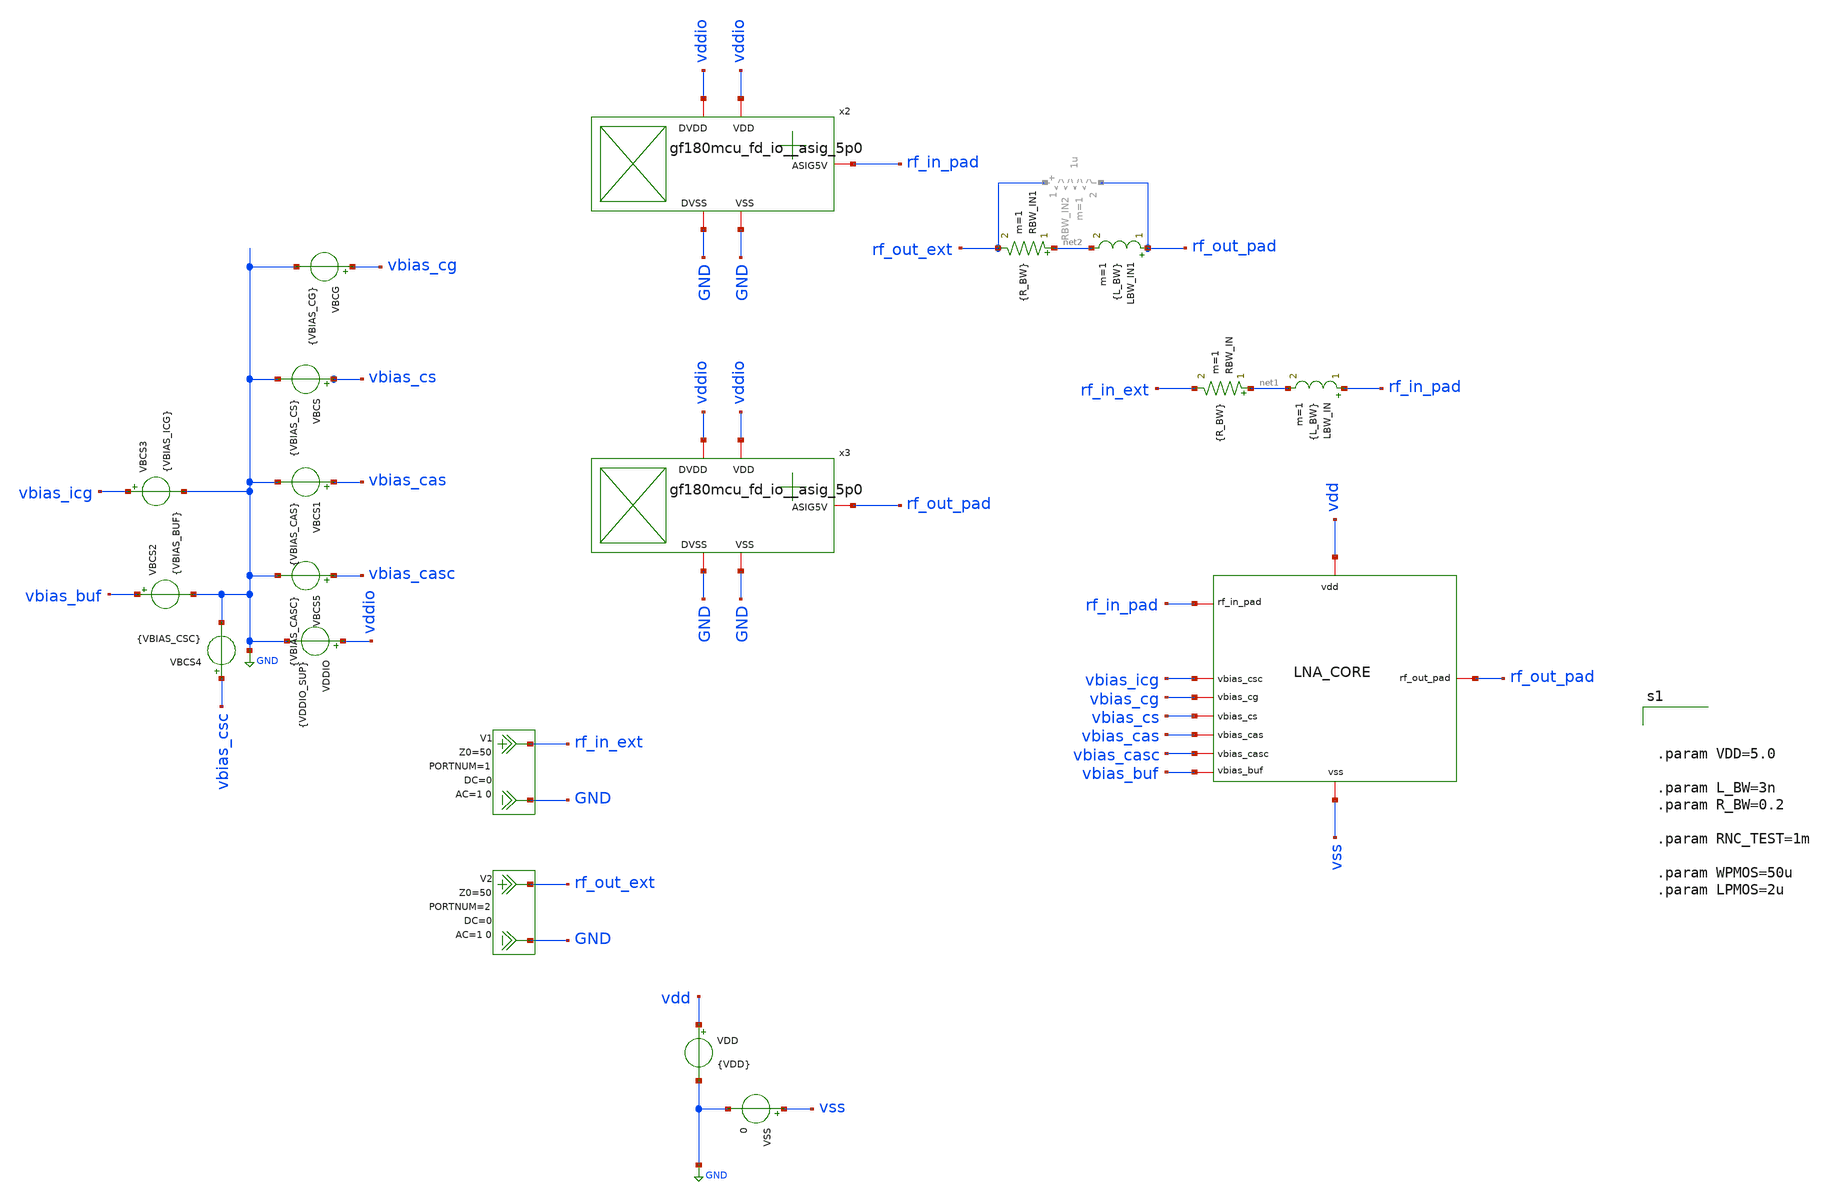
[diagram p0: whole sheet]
** sch_path: xschem/lna-core_tb.sch
**.subckt lna-core_tb
x1 vbias_cg rf_in_pad vbias_cs rf_out_pad vdd vbias_cas vss vbias_casc vbias_buf vbias_icg lna_core
VDD vdd GND {VDD}
VSS vss GND 0
LBW_IN rf_in_pad net1 {L_BW} m=1
RBW_IN net1 rf_in_ext {R_BW} m=1
LBW_IN1 rf_out_pad net2 {L_BW} m=1
RBW_IN1 net2 rf_out_ext {R_BW} m=1
VBCG vbias_cg GND {VBIAS_CG}
VDDIO vddio GND {VDDIO_SUP}
VBCS vbias_cs GND {VBIAS_CS}
VBCS1 vbias_cas GND {VBIAS_CAS}
VBCS2 vbias_buf GND {VBIAS_BUF}
VBCS3 vbias_icg GND {VBIAS_ICG}
VBCS4 vbias_csc GND {VBIAS_CSC}
VBCS5 vbias_casc GND {VBIAS_CASC}
V1 rf_in_ext GND DC 0 AC 1 0 portnum 1 z0 50
V2 rf_out_ext GND DC 0 AC 1 0 portnum 2 z0 50
x2 rf_in_pad vddio GND vddio GND gf180mcu_fd_io__asig_5p0
x3 rf_out_pad vddio GND vddio GND gf180mcu_fd_io__asig_5p0
**** begin user architecture code

.include $::180MCU_MODELS/design.ngspice
.lib $::180MCU_MODELS/sm141064.ngspice typical
.lib $::180MCU_MODELS/sm141064.ngspice cap_mim
.lib $::180MCU_MODELS/sm141064.ngspice res_typical
.lib $::180MCU_MODELS/sm141064.ngspice moscap_typical
.lib $::180MCU_MODELS/sm141064.ngspice mimcap_typical
.lib $::180MCU_MODELS/sm141064.ngspice diode_typical

.include $::env(PWD)/gf180mcu_fd_io__asig_5p0_pex__pdk_gf180mcuD__rcx__flat__cthresh_0__extresist_0mohm.spice

* ============================================================
* INDUCTOR MODEL SWEEP CONFIG -- change the shared section name
* (ideal / rl / snp2le) in all 4 lines below to switch every
* swept inductor's model at once, or run:
*   ./set_inductor_model.sh ideal_or_rl_or_snp2le
* from the xschem/ directory.
*   ideal  : single ideal inductor (L only)
*   rl     : EM-derived series L + equivalent series R
*   snp2le : snp2le broadband vector-fitted macromodel (passive,
*            DC-pinned, thermal-noise-synthesized), same EM data as rl
* ============================================================
.lib $::env(PWD)/LEQ_model.lib rl
.lib $::env(PWD)/LSHUNT_OUT_model.lib rl
.lib $::env(PWD)/LD2_model.lib rl
.lib $::env(PWD)/LD4_model.lib rl




.param VDD=5.0

.param L_BW=3n
.param R_BW=0.2

.param RNC_TEST=1m

.param WPMOS=50u
.param LPMOS=2u






.control

set noaskquit
set wr_singlescale
set wr_vecnames
set numdgt=10

let target_gain_bw=10.0

echo ============================================================ > lna_core_06V_cgcs_report.txt
echo GF180MCU_LNA_CORE_06V_CGCS_DETAILED_REPORT >> lna_core_06V_cgcs_report.txt
echo TARGET_FREQUENCY_HZ 2.400e9 >> lna_core_06V_cgcs_report.txt
echo TARGET_BAND_HZ 2.300e9 2.500e9 >> lna_core_06V_cgcs_report.txt
echo GAIN_BANDWIDTH_THRESHOLD_DB 10.0 >> lna_core_06V_cgcs_report.txt
echo PORT_REFERENCE_OHM 50 >> lna_core_06V_cgcs_report.txt
echo NOTE_HIERARCHY LNA_CORE_INSTANCE_IS_X1 >> lna_core_06V_cgcs_report.txt
echo ============================================================ >> lna_core_06V_cgcs_report.txt

* =============================================================================
* DC OPERATING POINT
* =============================================================================

op

* Top-level supply and bias-generator values.
let pdcop=1e3*abs(i(VDD))*v(vdd)
let icoreop=abs(i(VDD))
let iioop=0

let v_vddop=v(vdd)
let v_vpop=v(vp)
let v_vrefop=v(vref)
let v_vsenseop=v(vsense)
let v_vbias_casop=v(vbias_cas)
let v_vbias_3v3op=v(vbias_3v3)
let v_vbias_cascop=v(vbias_casc)
let v_vbias_cgop=v(vbias_cg)
let v_vbias_icgop=v(vbias_icg)
let v_vbias_bufop=v(vbias_buf)
let v_vbias_csop=v(vbias_cs)
let v_vbias_cscop=v(vbias_csc)

let i_r1=(v(vbias_cas)-v(vbias_3v3))/20k
let i_r2=(v(vbias_3v3)-v(vbias_casc))/5k
let i_r3=(v(vbias_casc)-v(vbias_cg))/50k
let i_r4=(v(vbias_cg)-v(vbias_icg))/15k
let i_r5=(v(vbias_icg)-v(vbias_buf))/30k
let i_r6=(v(vbias_buf)-v(vbias_cs))/5k
let i_r7=(v(vbias_cs)-v(vsense))/3.066k
let i_r8=(v(vsense)-v(vbias_csc))/11.934k
let i_r9=v(vbias_csc)/45k
let i_ladder_avg=(i_r1+i_r2+i_r3+i_r4+i_r5+i_r6+i_r7+i_r8+i_r9)/9

* LNA internal nodes are inside instance x1.
let vsop=v(x1.s)
let vdop=v(x1.vm2)
let vnet3op=v(x1.net3)
let vnet8op=v(x1.net8)
let vbufop=v(x1.vbuf)
let vgcsop=v(x1.g_cs)
let vgcgop=v(x1.g_cg)
let vgcsccop=v(x1.g_csc)
let vxop=v(x1.vx)
let vm1op=v(x1.vm1)
let vm2op=v(x1.vm2)

* XM1: main CS device.
let id1op=abs(@m.x1.xm1.m0[id])
let gm1op=@m.x1.xm1.m0[gm]
let gmb1op=@m.x1.xm1.m0[gmbs]
let gds1op=@m.x1.xm1.m0[gds]
let vgs1op=@m.x1.xm1.m0[vgs]
let vds1op=@m.x1.xm1.m0[vds]
let vbs1op=@m.x1.xm1.m0[vbs]
let vth1op=@m.x1.xm1.m0[vth]
let vov1op=vgs1op-vth1op
let vdsat1op=abs(@m.x1.xm1.m0[vdsat])
let sat1op=vds1op-vdsat1op
let gmid1op=gm1op/(id1op+1e-30)
let ro1op=1/(gds1op+1e-30)

* XM2: CG input device.
let id2op=abs(@m.x1.xm2.m0[id])
let gm2op=@m.x1.xm2.m0[gm]
let gmb2op=@m.x1.xm2.m0[gmbs]
let gds2op=@m.x1.xm2.m0[gds]
let vgs2op=@m.x1.xm2.m0[vgs]
let vds2op=@m.x1.xm2.m0[vds]
let vbs2op=@m.x1.xm2.m0[vbs]
let vth2op=@m.x1.xm2.m0[vth]
let vov2op=vgs2op-vth2op
let vdsat2op=abs(@m.x1.xm2.m0[vdsat])
let sat2op=vds2op-vdsat2op
let gmid2op=gm2op/(id2op+1e-30)
let ro2op=1/(gds2op+1e-30)

* XM3: source follower.
let id3op=abs(@m.x1.xm3.m0[id])
let gm3op=@m.x1.xm3.m0[gm]
let gmb3op=@m.x1.xm3.m0[gmbs]
let gds3op=@m.x1.xm3.m0[gds]
let vgs3op=@m.x1.xm3.m0[vgs]
let vds3op=@m.x1.xm3.m0[vds]
let vbs3op=@m.x1.xm3.m0[vbs]
let vth3op=@m.x1.xm3.m0[vth]
let vov3op=vgs3op-vth3op
let vdsat3op=abs(@m.x1.xm3.m0[vdsat])
let sat3op=vds3op-vdsat3op
let gmid3op=gm3op/(id3op+1e-30)
let ro3op=1/(gds3op+1e-30)

* XM4: CS cascode.
let id4op=abs(@m.x1.xm4.m0[id])
let gm4op=@m.x1.xm4.m0[gm]
let gmb4op=@m.x1.xm4.m0[gmbs]
let gds4op=@m.x1.xm4.m0[gds]
let vgs4op=@m.x1.xm4.m0[vgs]
let vds4op=@m.x1.xm4.m0[vds]
let vbs4op=@m.x1.xm4.m0[vbs]
let vth4op=@m.x1.xm4.m0[vth]
let vov4op=vgs4op-vth4op
let vdsat4op=abs(@m.x1.xm4.m0[vdsat])
let sat4op=vds4op-vdsat4op
let gmid4op=gm4op/(id4op+1e-30)
let ro4op=1/(gds4op+1e-30)

* XM5: CG current sink.
let id5op=abs(@m.x1.xm5.m0[id])
let gm5op=@m.x1.xm5.m0[gm]
let gmb5op=@m.x1.xm5.m0[gmbs]
let gds5op=@m.x1.xm5.m0[gds]
let vgs5op=@m.x1.xm5.m0[vgs]
let vds5op=@m.x1.xm5.m0[vds]
let vbs5op=@m.x1.xm5.m0[vbs]
let vth5op=@m.x1.xm5.m0[vth]
let vov5op=vgs5op-vth5op
let vdsat5op=abs(@m.x1.xm5.m0[vdsat])
let sat5op=vds5op-vdsat5op
let gmid5op=gm5op/(id5op+1e-30)
let ro5op=1/(gds5op+1e-30)

* XM6: buffer current sink.
let id6op=abs(@m.x1.xm6.m0[id])
let gm6op=@m.x1.xm6.m0[gm]
let gmb6op=@m.x1.xm6.m0[gmbs]
let gds6op=@m.x1.xm6.m0[gds]
let vgs6op=@m.x1.xm6.m0[vgs]
let vds6op=@m.x1.xm6.m0[vds]
let vbs6op=@m.x1.xm6.m0[vbs]
let vth6op=@m.x1.xm6.m0[vth]
let vov6op=vgs6op-vth6op
let vdsat6op=abs(@m.x1.xm6.m0[vdsat])
let sat6op=vds6op-vdsat6op
let gmid6op=gm6op/(id6op+1e-30)
let ro6op=1/(gds6op+1e-30)

* XM7: CG cascode.
let id7op=abs(@m.x1.xm7.m0[id])
let gm7op=@m.x1.xm7.m0[gm]
let gmb7op=@m.x1.xm7.m0[gmbs]
let gds7op=@m.x1.xm7.m0[gds]
let vgs7op=@m.x1.xm7.m0[vgs]
let vds7op=@m.x1.xm7.m0[vds]
let vbs7op=@m.x1.xm7.m0[vbs]
let vth7op=@m.x1.xm7.m0[vth]
let vov7op=vgs7op-vth7op
let vdsat7op=abs(@m.x1.xm7.m0[vdsat])
let sat7op=vds7op-vdsat7op
let gmid7op=gm7op/(id7op+1e-30)
let ro7op=1/(gds7op+1e-30)

* XM9: cancellation CS.
let id9op=abs(@m.x1.xm9.m0[id])
let gm9op=@m.x1.xm9.m0[gm]
let gmb9op=@m.x1.xm9.m0[gmbs]
let gds9op=@m.x1.xm9.m0[gds]
let vgs9op=@m.x1.xm9.m0[vgs]
let vds9op=@m.x1.xm9.m0[vds]
let vbs9op=@m.x1.xm9.m0[vbs]
let vth9op=@m.x1.xm9.m0[vth]
let vov9op=vgs9op-vth9op
let vdsat9op=abs(@m.x1.xm9.m0[vdsat])
let sat9op=vds9op-vdsat9op
let gmid9op=gm9op/(id9op+1e-30)
let ro9op=1/(gds9op+1e-30)

let vnet9op=vnet3op+vds1op
let vnet9check=vnet8op-vds4op
let vnet9diff=vnet9op-vnet9check
let vnet10op=vsop+vds2op
let vnet10check=vdop-vds7op
let vnet10diff=vnet10op-vnet10check

set op_pdc=$&pdcop
set op_icore=$&icoreop
set op_iio=$&iioop
set op_vs=$&vsop
set op_vnet10=$&vnet10op
set op_vnet10check=$&vnet10check
set op_vnet10diff=$&vnet10diff
set op_vd=$&vdop
set op_vnet3=$&vnet3op
set op_vnet9=$&vnet9op
set op_vnet9check=$&vnet9check
set op_vnet9diff=$&vnet9diff
set op_vnet8=$&vnet8op
set op_vbuf=$&vbufop
set op_vgcs=$&vgcsop
set op_vgcg=$&vgcgop
set op_vgcsc=$&vgcsccop
set op_vx=$&vxop
set op_vm1=$&vm1op
set op_vm2=$&vm2op

set op_vdd=$&v_vddop
set op_vp=$&v_vpop
set op_vref=$&v_vrefop
set op_vsense=$&v_vsenseop
set op_vbias_cas=$&v_vbias_casop
set op_vbias_3v3=$&v_vbias_3v3op
set op_vbias_casc=$&v_vbias_cascop
set op_vbias_cg=$&v_vbias_cgop
set op_vbias_icg=$&v_vbias_icgop
set op_vbias_buf=$&v_vbias_bufop
set op_vbias_cs=$&v_vbias_csop
set op_vbias_csc=$&v_vbias_cscop
set op_iladder=$&i_ladder_avg

set op_id1=$&id1op
set op_gm1=$&gm1op
set op_gmb1=$&gmb1op
set op_gds1=$&gds1op
set op_vgs1=$&vgs1op
set op_vds1=$&vds1op
set op_vbs1=$&vbs1op
set op_vth1=$&vth1op
set op_vov1=$&vov1op
set op_vdsat1=$&vdsat1op
set op_sat1=$&sat1op
set op_gmid1=$&gmid1op
set op_ro1=$&ro1op

set op_id2=$&id2op
set op_gm2=$&gm2op
set op_gmb2=$&gmb2op
set op_gds2=$&gds2op
set op_vgs2=$&vgs2op
set op_vds2=$&vds2op
set op_vbs2=$&vbs2op
set op_vth2=$&vth2op
set op_vov2=$&vov2op
set op_vdsat2=$&vdsat2op
set op_sat2=$&sat2op
set op_gmid2=$&gmid2op
set op_ro2=$&ro2op

set op_id3=$&id3op
set op_gm3=$&gm3op
set op_gmb3=$&gmb3op
set op_gds3=$&gds3op
set op_vgs3=$&vgs3op
set op_vds3=$&vds3op
set op_vbs3=$&vbs3op
set op_vth3=$&vth3op
set op_vov3=$&vov3op
set op_vdsat3=$&vdsat3op
set op_sat3=$&sat3op
set op_gmid3=$&gmid3op
set op_ro3=$&ro3op

set op_id4=$&id4op
set op_gm4=$&gm4op
set op_gmb4=$&gmb4op
set op_gds4=$&gds4op
set op_vgs4=$&vgs4op
set op_vds4=$&vds4op
set op_vbs4=$&vbs4op
set op_vth4=$&vth4op
set op_vov4=$&vov4op
set op_vdsat4=$&vdsat4op
set op_sat4=$&sat4op
set op_gmid4=$&gmid4op
set op_ro4=$&ro4op

set op_id5=$&id5op
set op_gm5=$&gm5op
set op_gmb5=$&gmb5op
set op_gds5=$&gds5op
set op_vgs5=$&vgs5op
set op_vds5=$&vds5op
set op_vbs5=$&vbs5op
set op_vth5=$&vth5op
set op_vov5=$&vov5op
set op_vdsat5=$&vdsat5op
set op_sat5=$&sat5op
set op_gmid5=$&gmid5op
set op_ro5=$&ro5op

set op_id6=$&id6op
set op_gm6=$&gm6op
set op_gmb6=$&gmb6op
set op_gds6=$&gds6op
set op_vgs6=$&vgs6op
set op_vds6=$&vds6op
set op_vbs6=$&vbs6op
set op_vth6=$&vth6op
set op_vov6=$&vov6op
set op_vdsat6=$&vdsat6op
set op_sat6=$&sat6op
set op_gmid6=$&gmid6op
set op_ro6=$&ro6op

set op_id7=$&id7op
set op_gm7=$&gm7op
set op_gmb7=$&gmb7op
set op_gds7=$&gds7op
set op_vgs7=$&vgs7op
set op_vds7=$&vds7op
set op_vbs7=$&vbs7op
set op_vth7=$&vth7op
set op_vov7=$&vov7op
set op_vdsat7=$&vdsat7op
set op_sat7=$&sat7op
set op_gmid7=$&gmid7op
set op_ro7=$&ro7op

set op_id9=$&id9op
set op_gm9=$&gm9op
set op_gmb9=$&gmb9op
set op_gds9=$&gds9op
set op_vgs9=$&vgs9op
set op_vds9=$&vds9op
set op_vbs9=$&vbs9op
set op_vth9=$&vth9op
set op_vov9=$&vov9op
set op_vdsat9=$&vdsat9op
set op_sat9=$&sat9op
set op_gmid9=$&gmid9op
set op_ro9=$&ro9op

echo ============================================================ >> lna_core_06V_cgcs_report.txt
echo DC_SUPPLY_AND_BIAS_GENERATOR >> lna_core_06V_cgcs_report.txt
echo PDC_mW $op_pdc ICORE_A $op_icore IIO_A $op_iio >> lna_core_06V_cgcs_report.txt
echo BIAS_TOP_LEVEL_V VDD $op_vdd VP_BANDGAP $op_vp OTA_OUT_VREF $op_vref VSENSE $op_vsense ILADDER_A $op_iladder >> lna_core_06V_cgcs_report.txt
echo BIAS_LADDER_V VBIAS_CAS $op_vbias_cas VBIAS_3V3 $op_vbias_3v3 VBIAS_CASC $op_vbias_casc VBIAS_CG $op_vbias_cg VBIAS_ICG $op_vbias_icg VBIAS_BUF $op_vbias_buf VBIAS_CS $op_vbias_cs VBIAS_CSC $op_vbias_csc >> lna_core_06V_cgcs_report.txt
echo ============================================================ >> lna_core_06V_cgcs_report.txt
echo DC_LNA_INTERNAL_NODE_VOLTAGES >> lna_core_06V_cgcs_report.txt
echo NODES_V S $op_vs VX $op_vx VM1 $op_vm1 VM2 $op_vm2 NET10_DERIVED $op_vnet10 NET3 $op_vnet3 NET9_DERIVED $op_vnet9 NET8 $op_vnet8 VBUF $op_vbuf G_CS $op_vgcs G_CG $op_vgcg G_CSC $op_vgcsc >> lna_core_06V_cgcs_report.txt
echo HIDDEN_NODE_CHECKS NET10_FROM_XM2 $op_vnet10 NET10_FROM_XM7 $op_vnet10check DIFFERENCE $op_vnet10diff NET9_FROM_XM1 $op_vnet9 NET9_FROM_XM4 $op_vnet9check DIFFERENCE $op_vnet9diff >> lna_core_06V_cgcs_report.txt
echo ============================================================ >> lna_core_06V_cgcs_report.txt
echo TRANSISTOR_OPERATING_POINTS >> lna_core_06V_cgcs_report.txt
echo FIELDS ID_A GM_S GMBS_S GDS_S VGS_V VDS_V VBS_V VTH_V VOV_V VDSAT_V SAT_MARGIN_V GM_OVER_ID_1_PER_V RO_OHM >> lna_core_06V_cgcs_report.txt
echo XM1_CS ID $op_id1 GM $op_gm1 GMBS $op_gmb1 GDS $op_gds1 VGS $op_vgs1 VDS $op_vds1 VBS $op_vbs1 VTH $op_vth1 VOV $op_vov1 VDSAT $op_vdsat1 SAT_MARGIN $op_sat1 GMID $op_gmid1 RO $op_ro1 >> lna_core_06V_cgcs_report.txt
echo XM2_CG ID $op_id2 GM $op_gm2 GMBS $op_gmb2 GDS $op_gds2 VGS $op_vgs2 VDS $op_vds2 VBS $op_vbs2 VTH $op_vth2 VOV $op_vov2 VDSAT $op_vdsat2 SAT_MARGIN $op_sat2 GMID $op_gmid2 RO $op_ro2 >> lna_core_06V_cgcs_report.txt
echo XM3_SOURCE_FOLLOWER ID $op_id3 GM $op_gm3 GMBS $op_gmb3 GDS $op_gds3 VGS $op_vgs3 VDS $op_vds3 VBS $op_vbs3 VTH $op_vth3 VOV $op_vov3 VDSAT $op_vdsat3 SAT_MARGIN $op_sat3 GMID $op_gmid3 RO $op_ro3 >> lna_core_06V_cgcs_report.txt
echo XM4_CS_CASCODE ID $op_id4 GM $op_gm4 GMBS $op_gmb4 GDS $op_gds4 VGS $op_vgs4 VDS $op_vds4 VBS $op_vbs4 VTH $op_vth4 VOV $op_vov4 VDSAT $op_vdsat4 SAT_MARGIN $op_sat4 GMID $op_gmid4 RO $op_ro4 >> lna_core_06V_cgcs_report.txt
echo XM5_CG_CURRENT_SINK ID $op_id5 GM $op_gm5 GMBS $op_gmb5 GDS $op_gds5 VGS $op_vgs5 VDS $op_vds5 VBS $op_vbs5 VTH $op_vth5 VOV $op_vov5 VDSAT $op_vdsat5 SAT_MARGIN $op_sat5 GMID $op_gmid5 RO $op_ro5 >> lna_core_06V_cgcs_report.txt
echo XM6_BUFFER_CURRENT_SINK ID $op_id6 GM $op_gm6 GMBS $op_gmb6 GDS $op_gds6 VGS $op_vgs6 VDS $op_vds6 VBS $op_vbs6 VTH $op_vth6 VOV $op_vov6 VDSAT $op_vdsat6 SAT_MARGIN $op_sat6 GMID $op_gmid6 RO $op_ro6 >> lna_core_06V_cgcs_report.txt
echo XM7_CG_CASCODE ID $op_id7 GM $op_gm7 GMBS $op_gmb7 GDS $op_gds7 VGS $op_vgs7 VDS $op_vds7 VBS $op_vbs7 VTH $op_vth7 VOV $op_vov7 VDSAT $op_vdsat7 SAT_MARGIN $op_sat7 GMID $op_gmid7 RO $op_ro7 >> lna_core_06V_cgcs_report.txt
echo XM9_CANCELLATION_CS ID $op_id9 GM $op_gm9 GMBS $op_gmb9 GDS $op_gds9 VGS $op_vgs9 VDS $op_vds9 VBS $op_vbs9 VTH $op_vth9 VOV $op_vov9 VDSAT $op_sat9 SAT_MARGIN $op_sat9 GMID $op_gmid9 RO $op_ro9 >> lna_core_06V_cgcs_report.txt

destroy $curplot

* =============================================================================
* SINGLE BROADBAND RF ANALYSIS
* One reset and one SP run are used for all 1 MHz to 7 GHz RF results.
* Target-band values are extracted from the same dataset.
* =============================================================================

reset
sp lin 101 500Meg 5Gig 1
set rfplot=$curplot

let fghz=frequency/1e9

let s11db=db(s_1_1)
let s21db=db(s_2_1)
let s12db=db(s_1_2)
let s22db=db(s_2_2)

let s11re=real(s_1_1)
let s11im=imag(s_1_1)
let s21re=real(s_2_1)
let s21im=imag(s_2_1)
let s12re=real(s_1_2)
let s12im=imag(s_1_2)
let s22re=real(s_2_2)
let s22im=imag(s_2_2)

let z22re=real(z_2_2)
let z22im=imag(z_2_2)

let nfdb=real(NF)
let nfmin_db=real(NFmin)

let delta=s_1_1*s_2_2-s_1_2*s_2_1
let delta_mag=mag(delta)
let a11=mag(s_1_1)
let a12=mag(s_1_2)
let a21=mag(s_2_1)
let a22=mag(s_2_2)
let mu=(1-a11*a11)/(mag(s_2_2-delta*conj(s_1_1))+mag(s_1_2*s_2_1))
let mup=(1-a22*a22)/(mag(s_1_1-delta*conj(s_2_2))+mag(s_1_2*s_2_1))
let kval=(1-a11*a11-a22*a22+delta_mag*delta_mag)/(2*a12*a21)

let zin=50*(1+s_1_1)/(1-s_1_1)
let zout=50*(1+s_2_2)/(1-s_2_2)
let zin_re=real(zin)
let zin_im=imag(zin)
let zout_re=real(zout)
let zout_im=imag(zout)

let npts=length(frequency)

let ilo=0
let icenter=0
let ihi=0
let errlo=abs(frequency[0]-2.3e9)
let errcenter=abs(frequency[0]-2.4e9)
let errhi=abs(frequency[0]-2.5e9)
let ii=1

while ii < npts
let newerr=abs(frequency[ii]-2.3e9)
if newerr < errlo
let errlo=newerr
let ilo=ii
end
let newerr=abs(frequency[ii]-2.4e9)
if newerr < errcenter
let errcenter=newerr
let icenter=ii
end
let newerr=abs(frequency[ii]-2.5e9)
if newerr < errhi
let errhi=newerr
let ihi=ii
end
let ii=ii+1
end

let center_freq=frequency[icenter]
let s11c=s11db[icenter]
let s21c=s21db[icenter]
let s12c=s12db[icenter]
let s22c=s22db[icenter]
let s11rc=s11re[icenter]
let s11ic=s11im[icenter]
let s21rc=s21re[icenter]
let s21ic=s21im[icenter]
let s12rc=s12re[icenter]
let s12ic=s12im[icenter]
let s22rc=s22re[icenter]
let s22ic=s22im[icenter]
let nfc=nfdb[icenter]
let nfminc=nfmin_db[icenter]
let muc=mu[icenter]
let mupc=mup[icenter]
let kc=kval[icenter]
let dmc=delta_mag[icenter]
let zinrc=zin_re[icenter]
let zinic=zin_im[icenter]
let zoutrc=zout_re[icenter]
let zoutic=zout_im[icenter]

let s11min=s11db[ilo]
let s11max=s11db[ilo]
let s21min=s21db[ilo]
let s21max=s21db[ilo]
let s12min=s12db[ilo]
let s12max=s12db[ilo]
let s22min=s22db[ilo]
let s22max=s22db[ilo]
let nfbandmin=nfdb[ilo]
let nfbandmax=nfdb[ilo]
let nfminbandmin=nfmin_db[ilo]
let nfminbandmax=nfmin_db[ilo]
let mumin=mu[ilo]
let mupmin=mup[ilo]
let kmin=kval[ilo]
let dmax=delta_mag[ilo]

let s11min_i=ilo
let s11max_i=ilo
let s21min_i=ilo
let s21max_i=ilo
let s12min_i=ilo
let s12max_i=ilo
let s22min_i=ilo
let s22max_i=ilo
let nfmin_i=ilo
let nfmax_i=ilo
let nfminpar_min_i=ilo
let nfminpar_max_i=ilo
let mumin_i=ilo
let mupmin_i=ilo
let kmin_i=ilo
let dmax_i=ilo

let ii=ilo
while ii <= ihi
if s11db[ii] < s11min
let s11min=s11db[ii]
let s11min_i=ii
end
if s11db[ii] > s11max
let s11max=s11db[ii]
let s11max_i=ii
end
if s21db[ii] < s21min
let s21min=s21db[ii]
let s21min_i=ii
end
if s21db[ii] > s21max
let s21max=s21db[ii]
let s21max_i=ii
end
if s12db[ii] < s12min
let s12min=s12db[ii]
let s12min_i=ii
end
if s12db[ii] > s12max
let s12max=s12db[ii]
let s12max_i=ii
end
if s22db[ii] < s22min
let s22min=s22db[ii]
let s22min_i=ii
end
if s22db[ii] > s22max
let s22max=s22db[ii]
let s22max_i=ii
end
if nfdb[ii] < nfbandmin
let nfbandmin=nfdb[ii]
let nfmin_i=ii
end
if nfdb[ii] > nfbandmax
let nfbandmax=nfdb[ii]
let nfmax_i=ii
end
if nfmin_db[ii] < nfminbandmin
let nfminbandmin=nfmin_db[ii]
let nfminpar_min_i=ii
end
if nfmin_db[ii] > nfminbandmax
let nfminbandmax=nfmin_db[ii]
let nfminpar_max_i=ii
end
if mu[ii] < mumin
let mumin=mu[ii]
let mumin_i=ii
end
if mup[ii] < mupmin
let mupmin=mup[ii]
let mupmin_i=ii
end
if kval[ii] < kmin
let kmin=kval[ii]
let kmin_i=ii
end
if delta_mag[ii] > dmax
let dmax=delta_mag[ii]
let dmax_i=ii
end
let ii=ii+1
end

let gain_ripple=s21max-s21min

let s11min_f=frequency[s11min_i]
let s11max_f=frequency[s11max_i]
let s21min_f=frequency[s21min_i]
let s21max_f=frequency[s21max_i]
let s12min_f=frequency[s12min_i]
let s12max_f=frequency[s12max_i]
let s22min_f=frequency[s22min_i]
let s22max_f=frequency[s22max_i]
let nfmin_f=frequency[nfmin_i]
let nfmax_f=frequency[nfmax_i]
let nfminpar_min_f=frequency[nfminpar_min_i]
let nfminpar_max_f=frequency[nfminpar_max_i]
let mumin_f=frequency[mumin_i]
let mupmin_f=frequency[mupmin_i]
let kmin_f=frequency[kmin_i]
let dmax_f=frequency[dmax_i]

let imax=0
let gainmax=s21db[0]
let ii=1
while ii < npts
if s21db[ii] > gainmax
let gainmax=s21db[ii]
let imax=ii
end
let ii=ii+1
end
let peakfreq=frequency[imax]

echo ============================================================ >> lna_core_06V_cgcs_report.txt
echo RF_AT_2P400_GHZ_FROM_SINGLE_BROADBAND_SWEEP >> lna_core_06V_cgcs_report.txt
echo ACTUAL_SAMPLE_HZ $&center_freq >> lna_core_06V_cgcs_report.txt
echo S11_DB $&s11c REAL $&s11rc IMAG $&s11ic >> lna_core_06V_cgcs_report.txt
echo S21_DB $&s21c REAL $&s21rc IMAG $&s21ic >> lna_core_06V_cgcs_report.txt
echo S12_DB $&s12c REAL $&s12rc IMAG $&s12ic >> lna_core_06V_cgcs_report.txt
echo S22_DB $&s22c REAL $&s22rc IMAG $&s22ic >> lna_core_06V_cgcs_report.txt
echo NF_DB $&nfc NFMIN_DB $&nfminc >> lna_core_06V_cgcs_report.txt
echo MU $&muc MUP $&mupc K $&kc DELTA_MAG $&dmc >> lna_core_06V_cgcs_report.txt
echo ZIN_OHM RE $&zinrc IM $&zinic >> lna_core_06V_cgcs_report.txt
echo ZOUT_OHM RE $&zoutrc IM $&zoutic >> lna_core_06V_cgcs_report.txt

echo ============================================================ >> lna_core_06V_cgcs_report.txt
echo RF_MIN_MAX_FROM_2P300_TO_2P500_GHZ >> lna_core_06V_cgcs_report.txt
echo S11_MIN_DB $&s11min AT_HZ $&s11min_f S11_MAX_DB $&s11max AT_HZ $&s11max_f >> lna_core_06V_cgcs_report.txt
echo S21_MIN_DB $&s21min AT_HZ $&s21min_f S21_MAX_DB $&s21max AT_HZ $&s21max_f GAIN_RIPPLE_DB $&gain_ripple >> lna_core_06V_cgcs_report.txt
echo S12_MIN_DB $&s12min AT_HZ $&s12min_f S12_MAX_DB $&s12max AT_HZ $&s12max_f >> lna_core_06V_cgcs_report.txt
echo S22_MIN_DB $&s22min AT_HZ $&s22min_f S22_MAX_DB $&s22max AT_HZ $&s22max_f >> lna_core_06V_cgcs_report.txt
echo NF_MIN_DB $&nfbandmin AT_HZ $&nfmin_f NF_MAX_DB $&nfbandmax AT_HZ $&nfmax_f >> lna_core_06V_cgcs_report.txt
echo NFMIN_PARAMETER_MIN_DB $&nfminbandmin AT_HZ $&nfminpar_min_f NFMIN_PARAMETER_MAX_DB $&nfminbandmax AT_HZ $&nfminpar_max_f >> lna_core_06V_cgcs_report.txt
echo MU_MIN $&mumin AT_HZ $&mumin_f MUP_MIN $&mupmin AT_HZ $&mupmin_f >> lna_core_06V_cgcs_report.txt
echo K_MIN $&kmin AT_HZ $&kmin_f DELTA_MAX $&dmax AT_HZ $&dmax_f >> lna_core_06V_cgcs_report.txt

echo ============================================================ >> lna_core_06V_cgcs_report.txt
echo BROADBAND_GAIN_CHECK_1MHZ_TO_7GHZ >> lna_core_06V_cgcs_report.txt
echo GAIN_AT_2P4_DB $&s21c >> lna_core_06V_cgcs_report.txt
echo BROADBAND_PEAK_HZ $&peakfreq PEAK_GAIN_DB $&gainmax >> lna_core_06V_cgcs_report.txt

echo ============================================================ >> lna_core_06V_cgcs_report.txt
echo TARGET_CENTERED_S21_GE_10DB_BAND >> lna_core_06V_cgcs_report.txt
if s21c >= 10.0
let bwlo=icenter
let bwhi=icenter
let search=1
while search = 1
if bwlo > 0
if s21db[bwlo-1] >= 10.0
let bwlo=bwlo-1
else
let search=0
end
else
let search=0
end
end
let search=1
while search = 1
if bwhi < npts-1
if s21db[bwhi+1] >= 10.0
let bwhi=bwhi+1
else
let search=0
end
else
let search=0
end
end
let bwflo=frequency[bwlo]
let bwfhi=frequency[bwhi]
let bwval=bwfhi-bwflo
let bwcenter=0.5*(bwfhi+bwflo)
let bwfbw=100*bwval/(bwcenter+1e-30)
echo LOWER_HZ $&bwflo UPPER_HZ $&bwfhi BANDWIDTH_HZ $&bwval BAND_CENTER_HZ $&bwcenter FRACTIONAL_BW_PERCENT $&bwfbw >> lna_core_06V_cgcs_report.txt
else
echo NO_VALID_TARGET_CENTERED_BAND S21_AT_2P4_DB $&s21c >> lna_core_06V_cgcs_report.txt
end

echo ============================================================ >> lna_core_06V_cgcs_report.txt
echo GLOBAL_CONTIGUOUS_S21_GE_10DB_BAND_AROUND_PEAK >> lna_core_06V_cgcs_report.txt
if gainmax >= 10.0
let bwlo=imax
let bwhi=imax
let search=1
while search = 1
if bwlo > 0
if s21db[bwlo-1] >= 10.0
let bwlo=bwlo-1
else
let search=0
end
else
let search=0
end
end
let search=1
while search = 1
if bwhi < npts-1
if s21db[bwhi+1] >= 10.0
let bwhi=bwhi+1
else
let search=0
end
else
let search=0
end
end
let bwflo=frequency[bwlo]
let bwfhi=frequency[bwhi]
let bwval=bwfhi-bwflo
let bwcenter=0.5*(bwfhi+bwflo)
let bwfbw=100*bwval/(bwcenter+1e-30)
echo LOWER_HZ $&bwflo UPPER_HZ $&bwfhi BANDWIDTH_HZ $&bwval BAND_CENTER_HZ $&bwcenter FRACTIONAL_BW_PERCENT $&bwfbw >> lna_core_06V_cgcs_report.txt
else
echo NO_S21_ABOVE_10DB_FROM_1MHZ_TO_7GHZ PEAK_GAIN_DB $&gainmax PEAK_FREQUENCY_HZ $&peakfreq >> lna_core_06V_cgcs_report.txt
end

wrdata lna_core_06V_cgcs_target_band.dat frequency s_1_1 s_2_1 s_1_2 s_2_2 s11db s21db s12db s22db nfdb nfmin_db kval mu mup delta_mag zin_re zin_im zout_re zout_im
wrdata lna_core_06V_cgcs_broadband.dat frequency s11db s21db s12db s22db nfdb nfmin_db kval mu mup delta_mag zin_re zin_im zout_re zout_im

* =============================================================================
* NOISE-CANCELLATION A/B PROOF
* Same method as before. For this to work, XC10 must use:
* c_width={CNC_WIDTH} c_length={CNC_LENGTH}
* =============================================================================

set nc_on_plot=$rfplot

alterparam CNC_WIDTH = 1e-6u
alterparam CNC_LENGTH = 1e-6u
reset

sp lin 101 500Meg 5Gig 1
set nc_off_plot=$curplot

let fghz_nc=frequency/1e9

let nf_nc_on={$nc_on_plot}.nfdb
let s21_nc_on={$nc_on_plot}.s21db
let s11_nc_on={$nc_on_plot}.s11db
let s22_nc_on={$nc_on_plot}.s22db

let nf_nc_off=real(NF)
let s21_nc_off=db(s_2_1)
let s11_nc_off=db(s_1_1)
let s22_nc_off=db(s_2_2)

let nf_improvement_db=nf_nc_off-nf_nc_on
let gain_change_on_minus_off_db=s21_nc_on-s21_nc_off

let nc_npts=length(frequency)

let nc_ilo=0
let nc_icenter=0
let nc_ihi=0
let nc_errlo=abs(frequency[0]-2.3e9)
let nc_errcenter=abs(frequency[0]-2.4e9)
let nc_errhi=abs(frequency[0]-2.5e9)
let nc_ii=1

while nc_ii < nc_npts
let nc_newerr=abs(frequency[nc_ii]-2.3e9)
if nc_newerr < nc_errlo
let nc_errlo=nc_newerr
let nc_ilo=nc_ii
end
let nc_newerr=abs(frequency[nc_ii]-2.4e9)
if nc_newerr < nc_errcenter
let nc_errcenter=nc_newerr
let nc_icenter=nc_ii
end
let nc_newerr=abs(frequency[nc_ii]-2.5e9)
if nc_newerr < nc_errhi
let nc_errhi=nc_newerr
let nc_ihi=nc_ii
end
let nc_ii=nc_ii+1
end

let nc_freq_center=frequency[nc_icenter]
let nc_nf_on_c=nf_nc_on[nc_icenter]
let nc_nf_off_c=nf_nc_off[nc_icenter]
let nc_imp_c=nf_improvement_db[nc_icenter]

let nc_s21_on_c=s21_nc_on[nc_icenter]
let nc_s21_off_c=s21_nc_off[nc_icenter]
let nc_gain_delta_c=gain_change_on_minus_off_db[nc_icenter]

let nc_s11_on_c=s11_nc_on[nc_icenter]
let nc_s11_off_c=s11_nc_off[nc_icenter]
let nc_s22_on_c=s22_nc_on[nc_icenter]
let nc_s22_off_c=s22_nc_off[nc_icenter]

let nc_imp_min=nf_improvement_db[nc_ilo]
let nc_imp_max=nf_improvement_db[nc_ilo]
let nc_imp_min_i=nc_ilo
let nc_imp_max_i=nc_ilo

let nc_ii=nc_ilo
while nc_ii <= nc_ihi
if nf_improvement_db[nc_ii] < nc_imp_min
let nc_imp_min=nf_improvement_db[nc_ii]
let nc_imp_min_i=nc_ii
end
if nf_improvement_db[nc_ii] > nc_imp_max
let nc_imp_max=nf_improvement_db[nc_ii]
let nc_imp_max_i=nc_ii
end
let nc_ii=nc_ii+1
end

let nc_imp_min_f=frequency[nc_imp_min_i]
let nc_imp_max_f=frequency[nc_imp_max_i]

let nc_practical_threshold_db=0.20

echo ============================================================ >> lna_core_06V_cgcs_report.txt
echo NOISE_CANCELLATION_AB_PROOF >> lna_core_06V_cgcs_report.txt
echo METHOD ON_CNC_8P2PF OFF_CNC_1E_MINUS18F_XM7_XM9_STILL_BIASED_AND_LOADING_RETAINED >> lna_core_06V_cgcs_report.txt
echo ACTUAL_CENTER_SAMPLE_HZ $&nc_freq_center >> lna_core_06V_cgcs_report.txt
echo NF_ON_DB $&nc_nf_on_c NF_OFF_DB $&nc_nf_off_c NF_IMPROVEMENT_DB $&nc_imp_c >> lna_core_06V_cgcs_report.txt
echo S21_ON_DB $&nc_s21_on_c S21_OFF_DB $&nc_s21_off_c S21_ON_MINUS_OFF_DB $&nc_gain_delta_c >> lna_core_06V_cgcs_report.txt
echo S11_ON_DB $&nc_s11_on_c S11_OFF_DB $&nc_s11_off_c >> lna_core_06V_cgcs_report.txt
echo S22_ON_DB $&nc_s22_on_c S22_OFF_DB $&nc_s22_off_c >> lna_core_06V_cgcs_report.txt
echo NF_IMPROVEMENT_MIN_DB_2P3_TO_2P5 $&nc_imp_min AT_HZ $&nc_imp_min_f >> lna_core_06V_cgcs_report.txt
echo NF_IMPROVEMENT_MAX_DB_2P3_TO_2P5 $&nc_imp_max AT_HZ $&nc_imp_max_f >> lna_core_06V_cgcs_report.txt
echo PRACTICAL_CENTER_THRESHOLD_DB $&nc_practical_threshold_db >> lna_core_06V_cgcs_report.txt

if nc_imp_c > 0
echo CENTER_DIRECTIONAL_TEST PASS_CANCELLATION_LOWERS_NF >> lna_core_06V_cgcs_report.txt
else
echo CENTER_DIRECTIONAL_TEST FAIL_CANCELLATION_DOES_NOT_LOWER_NF >> lna_core_06V_cgcs_report.txt
end

if nc_imp_min > 0
echo FULL_TARGET_BAND_TEST PASS_CANCELLATION_LOWERS_NF_ACROSS_2P3_TO_2P5_GHZ >> lna_core_06V_cgcs_report.txt
else
echo FULL_TARGET_BAND_TEST FAIL_NF_IMPROVEMENT_NOT_POSITIVE_ACROSS_ENTIRE_TARGET_BAND >> lna_core_06V_cgcs_report.txt
end

if nc_imp_c >= nc_practical_threshold_db
echo PRACTICAL_CENTER_TEST PASS_IMPROVEMENT_AT_LEAST_0P20_DB >> lna_core_06V_cgcs_report.txt
else
echo PRACTICAL_CENTER_TEST FAIL_IMPROVEMENT_BELOW_0P20_DB >> lna_core_06V_cgcs_report.txt
end

wrdata lna_core_06V_cgcs_noise_cancellation.dat nf_nc_on nf_nc_off nf_improvement_db s21_nc_on s21_nc_off s11_nc_on s11_nc_off s22_nc_on s22_nc_off

alterparam CNC_WIDTH = 63.9529u
alterparam CNC_LENGTH = 63.9529u
reset

* =============================================================================
* WIDEBAND STABILITY 10 MHZ TO 30 GHZ
* =============================================================================

sp dec 11 100Meg 10G 1
set stabilityplot=$curplot

let wbdelta=s_1_1*s_2_2-s_1_2*s_2_1
let wbmd=mag(wbdelta)
let wba11=mag(s_1_1)
let wba12=mag(s_1_2)
let wba21=mag(s_2_1)
let wba22=mag(s_2_2)
let wbmu=(1-wba11*wba11)/(mag(s_2_2-wbdelta*conj(s_1_1))+mag(s_1_2*s_2_1))
let wbmup=(1-wba22*wba22)/(mag(s_1_1-wbdelta*conj(s_2_2))+mag(s_1_2*s_2_1))
let wbk=(1-wba11*wba11-wba22*wba22+wbmd*wbmd)/(2*wba12*wba21)

let wbkmin=minimum(wbk)
let wbmumin=minimum(wbmu)
let wbmupmin=minimum(wbmup)
let wbdmax=maximum(wbmd)

set final_wbkmin=$&wbkmin
set final_wbmumin=$&wbmumin
set final_wbmupmin=$&wbmupmin
set final_wbdmax=$&wbdmax

echo ============================================================ >> lna_core_06V_cgcs_report.txt
echo WIDEBAND_STABILITY_10MHZ_TO_30GHZ >> lna_core_06V_cgcs_report.txt
echo K_MIN $final_wbkmin MU_MIN $final_wbmumin MUP_MIN $final_wbmupmin DELTA_MAX $final_wbdmax >> lna_core_06V_cgcs_report.txt

wrdata lna_core_06V_cgcs_stability.dat frequency wbk wbmu wbmup wbmd

let wbfghz=frequency/1e9

echo ============================================================ >> lna_core_06V_cgcs_report.txt
echo OUTPUT_FILES >> lna_core_06V_cgcs_report.txt
echo REPORT lna_core_06V_cgcs_report.txt >> lna_core_06V_cgcs_report.txt
echo TARGET_DATA lna_core_06V_cgcs_target_band.dat >> lna_core_06V_cgcs_report.txt
echo BROADBAND_DATA lna_core_06V_cgcs_broadband.dat >> lna_core_06V_cgcs_report.txt
echo STABILITY_DATA lna_core_06V_cgcs_stability.dat >> lna_core_06V_cgcs_report.txt
echo NOISE_CANCELLATION_DATA lna_core_06V_cgcs_noise_cancellation.dat >> lna_core_06V_cgcs_report.txt
echo PLOTS S_PARAMETERS NF_NFMIN NOISE_CANCELLATION_ON_OFF NF_IMPROVEMENT S21_ON_OFF >> lna_core_06V_cgcs_report.txt
echo ============================================================ >> lna_core_06V_cgcs_report.txt

* =============================================================================
* VISIBLE PLOTS
* =============================================================================

setplot $rfplot
setscale fghz

*plot s11db xlimit 2.3 2.5
*plot s21db xlimit 2.3 2.5
*plot s12db xlimit 2.3 2.5
*plot s22db xlimit 2.3 2.5
*plot nfdb nfmin_db xlimit 2.3 2.5

plot s11db s22db s21db xlimit 0.5 5 ylimit -30 30
plot s11re s11im xlimit 2.2 2.6 ylimit -1 1
*plot z22re z22im xlimit 0.5 5
*plot s21db xlimit 0 7
*plot s12db xlimit 0 7
*plot s22db xlimit 0 7
plot nfdb nfmin_db xlimit 0.5 5 ylimit 0 5

setplot $nc_off_plot
setscale fghz_nc
set xbrushwidth=2

*plot nf_nc_on nf_nc_off xlimit 2.3 2.5 xlabel 'Frequency (GHz)' ylabel 'Noise figure (dB)'
*plot nf_improvement_db xlimit 2.3 2.5 xlabel 'Frequency (GHz)' ylabel 'NF OFF - NF ON (dB)'
*plot s21_nc_on s21_nc_off xlimit 2.3 2.5 xlabel 'Frequency (GHz)' ylabel 'S21 (dB)'

.endc




.param VBIAS_CAS_CG=3.30



.param VDS=5.0
.param VDDIO_SUP=5.0


.param VBIAS_CG=1.00
.param VBIAS_CS=1.20

.param VBIAS_CAS=3.70
.param VBIAS_ICG=1.90
.param VBIAS_BUF=1.30

.param VBIAS_CSC=0.90


.param VBIAS_CASC=3.20
.param RNC_TEST=1m



**** end user architecture code
**.ends
.GLOBAL GND
.end
